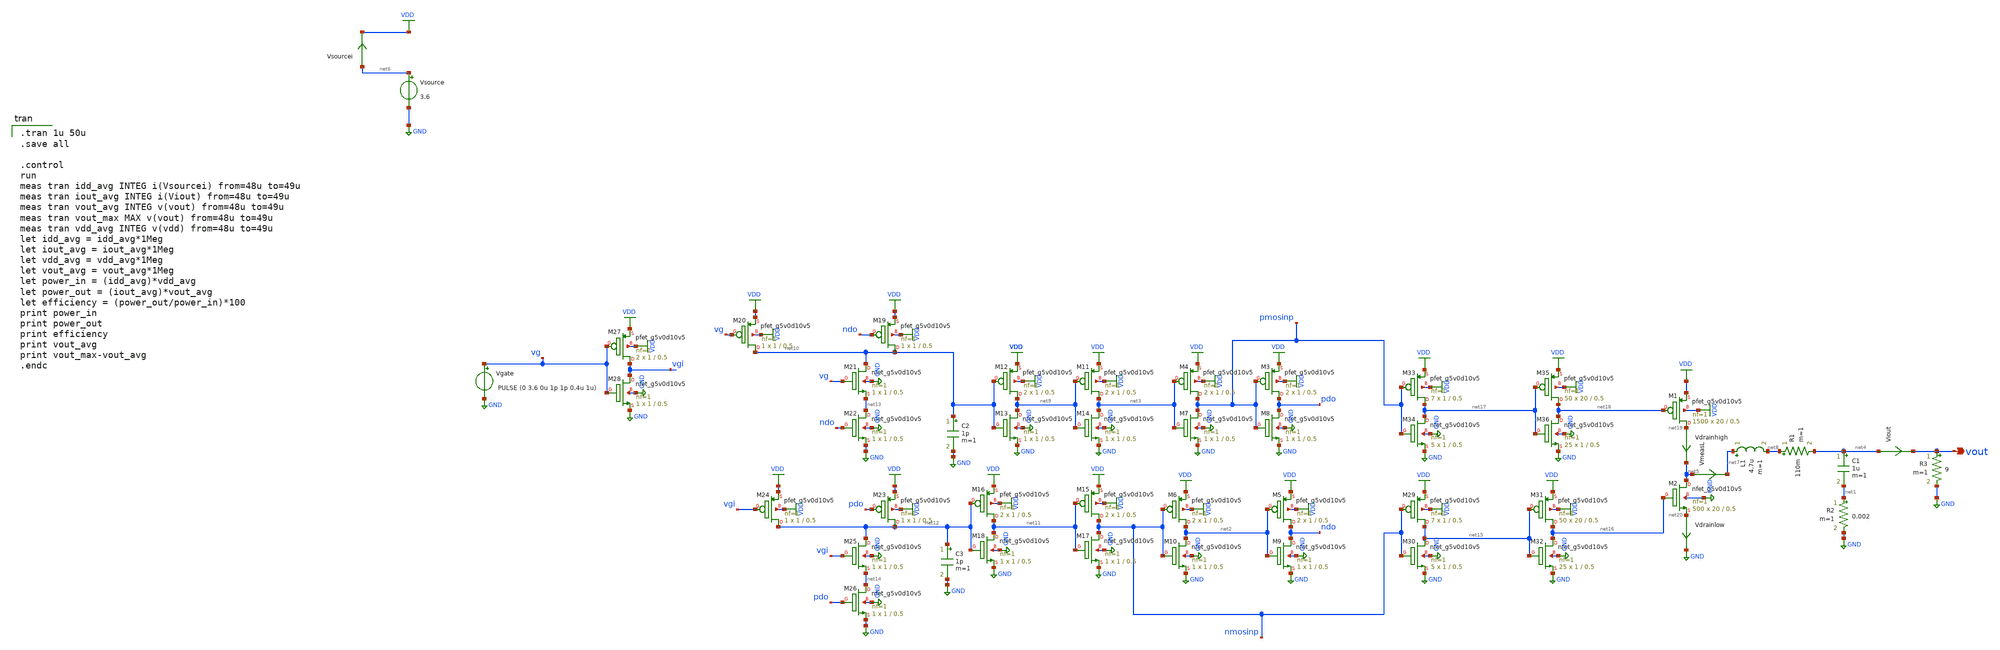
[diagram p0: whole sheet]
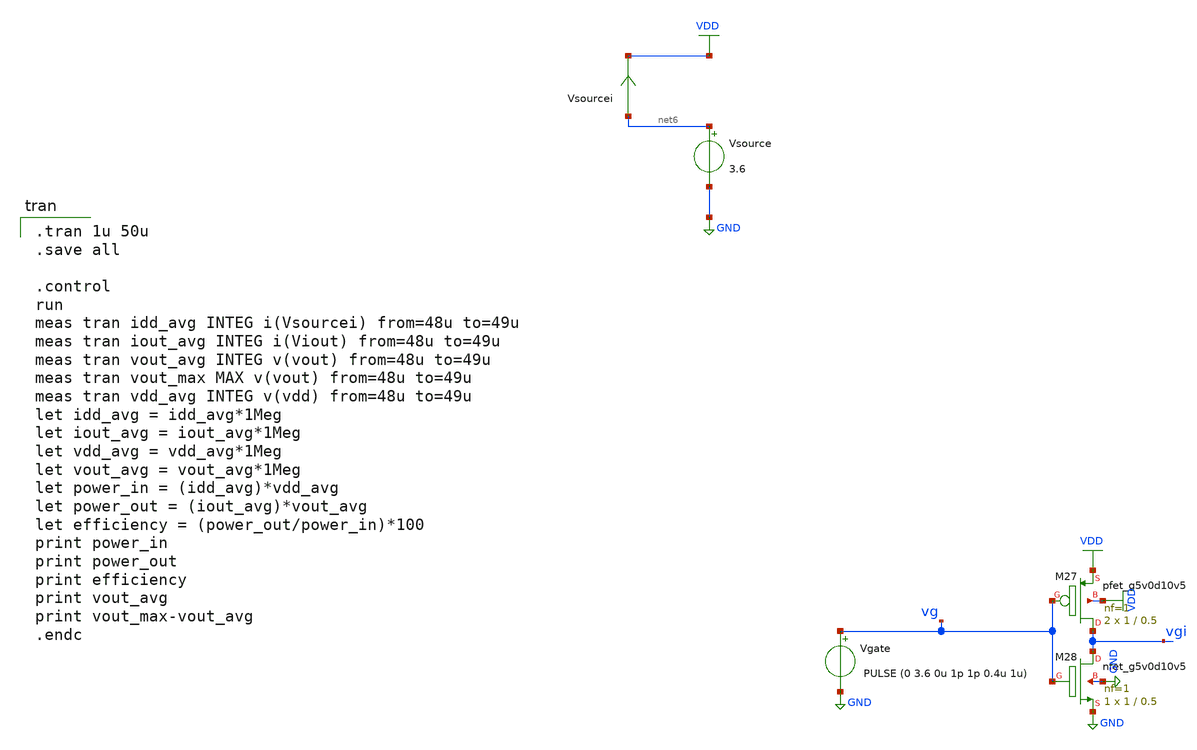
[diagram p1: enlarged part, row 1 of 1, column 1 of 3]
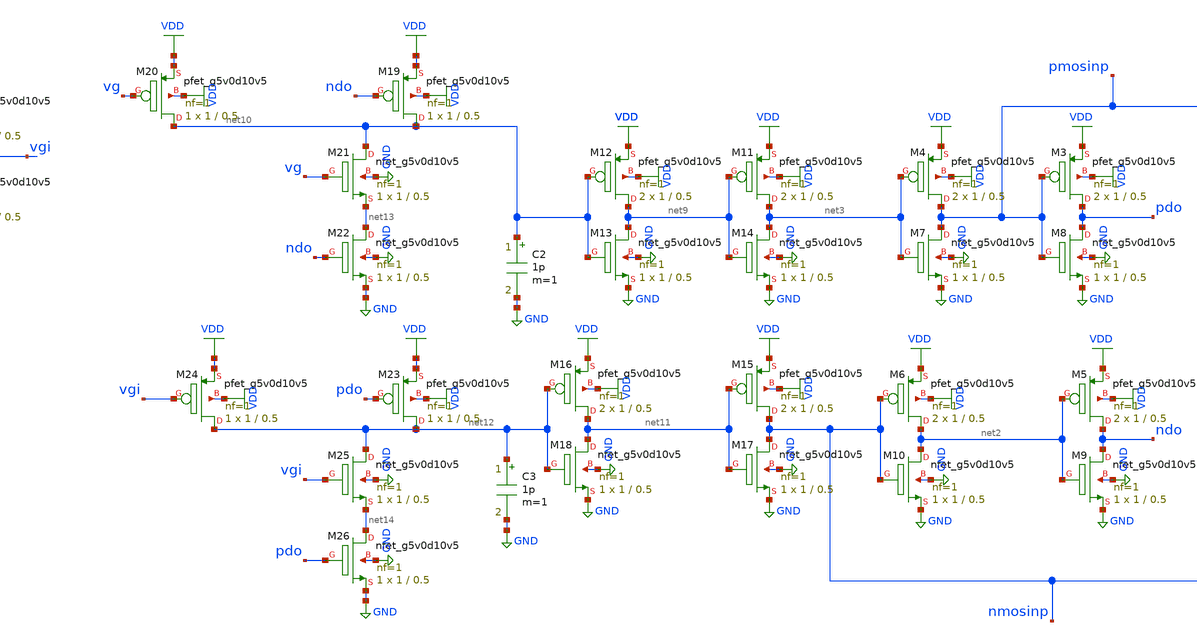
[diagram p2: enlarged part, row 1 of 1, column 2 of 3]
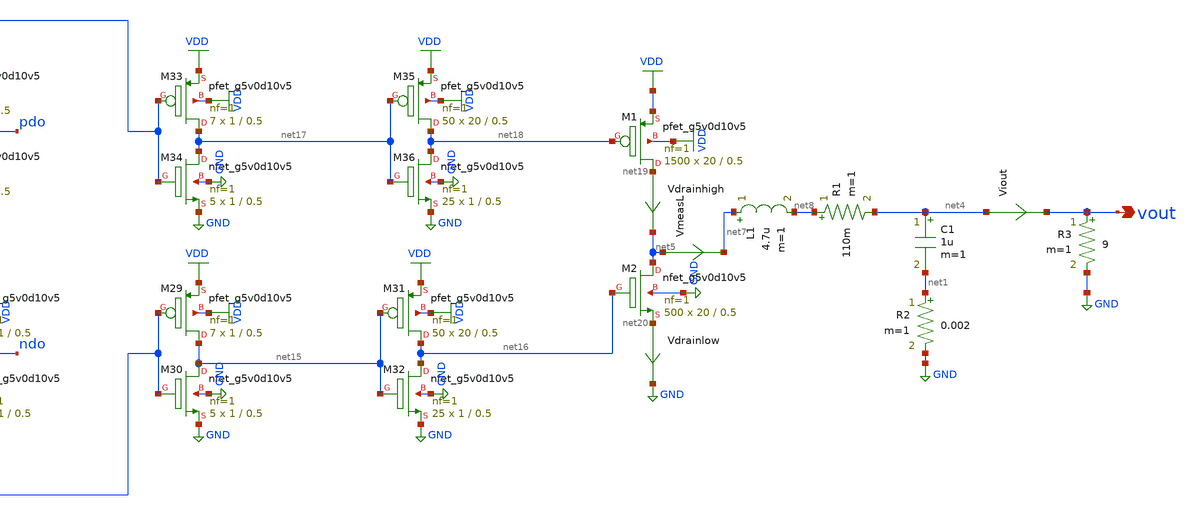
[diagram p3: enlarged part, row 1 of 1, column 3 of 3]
** sch_path: SMPS_With_Deadtime/buck_converter.sch
**.subckt buck_converter vout
*.opin vout
XM1 net19 net18 VDD VDD sky130_fd_pr__pfet_g5v0d10v5 L=0.5 W=20 nf=1 ad='int((nf+1)/2) * W/nf * 0.29'
+ as='int((nf+2)/2) * W/nf * 0.29' pd='2*int((nf+1)/2) * (W/nf + 0.29)' ps='2*int((nf+2)/2) * (W/nf + 0.29)'
+ nrd='0.29 / W' nrs='0.29 / W' sa=0 sb=0 sd=0 mult=1500 m=1500
XM2 net5 net16 net20 GND sky130_fd_pr__nfet_g5v0d10v5 L=0.5 W=20 nf=1 ad='int((nf+1)/2) * W/nf * 0.29'
+ as='int((nf+2)/2) * W/nf * 0.29' pd='2*int((nf+1)/2) * (W/nf + 0.29)' ps='2*int((nf+2)/2) * (W/nf + 0.29)'
+ nrd='0.29 / W' nrs='0.29 / W' sa=0 sb=0 sd=0 mult=500 m=500
L1 net7 net8 4.7u m=1
R1 net8 net4 110m m=1
C1 net4 net1 1u m=1
R2 net1 GND 0.002 m=1
Vgate vg GND PULSE (0 3.6 0u 1p 1p 0.4u 1u)
Vsource net6 GND 3.6
XM3 pdo pmosinp VDD VDD sky130_fd_pr__pfet_g5v0d10v5 L=0.5 W=1 nf=1 ad='int((nf+1)/2) * W/nf * 0.29'
+ as='int((nf+2)/2) * W/nf * 0.29' pd='2*int((nf+1)/2) * (W/nf + 0.29)' ps='2*int((nf+2)/2) * (W/nf + 0.29)'
+ nrd='0.29 / W' nrs='0.29 / W' sa=0 sb=0 sd=0 mult=2 m=2
XM4 pmosinp net3 VDD VDD sky130_fd_pr__pfet_g5v0d10v5 L=0.5 W=1 nf=1 ad='int((nf+1)/2) * W/nf * 0.29'
+ as='int((nf+2)/2) * W/nf * 0.29' pd='2*int((nf+1)/2) * (W/nf + 0.29)' ps='2*int((nf+2)/2) * (W/nf + 0.29)'
+ nrd='0.29 / W' nrs='0.29 / W' sa=0 sb=0 sd=0 mult=2 m=2
XM5 ndo net2 VDD VDD sky130_fd_pr__pfet_g5v0d10v5 L=0.5 W=1 nf=1 ad='int((nf+1)/2) * W/nf * 0.29' as='int((nf+2)/2) * W/nf * 0.29'
+ pd='2*int((nf+1)/2) * (W/nf + 0.29)' ps='2*int((nf+2)/2) * (W/nf + 0.29)' nrd='0.29 / W' nrs='0.29 / W'
+ sa=0 sb=0 sd=0 mult=2 m=2
XM6 net2 nmosinp VDD VDD sky130_fd_pr__pfet_g5v0d10v5 L=0.5 W=1 nf=1 ad='int((nf+1)/2) * W/nf * 0.29'
+ as='int((nf+2)/2) * W/nf * 0.29' pd='2*int((nf+1)/2) * (W/nf + 0.29)' ps='2*int((nf+2)/2) * (W/nf + 0.29)'
+ nrd='0.29 / W' nrs='0.29 / W' sa=0 sb=0 sd=0 mult=2 m=2
XM7 pmosinp net3 GND GND sky130_fd_pr__nfet_g5v0d10v5 L=0.5 W=1 nf=1 ad='int((nf+1)/2) * W/nf * 0.29'
+ as='int((nf+2)/2) * W/nf * 0.29' pd='2*int((nf+1)/2) * (W/nf + 0.29)' ps='2*int((nf+2)/2) * (W/nf + 0.29)'
+ nrd='0.29 / W' nrs='0.29 / W' sa=0 sb=0 sd=0 mult=1 m=1
XM8 pdo pmosinp GND GND sky130_fd_pr__nfet_g5v0d10v5 L=0.5 W=1 nf=1 ad='int((nf+1)/2) * W/nf * 0.29'
+ as='int((nf+2)/2) * W/nf * 0.29' pd='2*int((nf+1)/2) * (W/nf + 0.29)' ps='2*int((nf+2)/2) * (W/nf + 0.29)'
+ nrd='0.29 / W' nrs='0.29 / W' sa=0 sb=0 sd=0 mult=1 m=1
XM9 ndo net2 GND GND sky130_fd_pr__nfet_g5v0d10v5 L=0.5 W=1 nf=1 ad='int((nf+1)/2) * W/nf * 0.29' as='int((nf+2)/2) * W/nf * 0.29'
+ pd='2*int((nf+1)/2) * (W/nf + 0.29)' ps='2*int((nf+2)/2) * (W/nf + 0.29)' nrd='0.29 / W' nrs='0.29 / W'
+ sa=0 sb=0 sd=0 mult=1 m=1
XM10 net2 nmosinp GND GND sky130_fd_pr__nfet_g5v0d10v5 L=0.5 W=1 nf=1 ad='int((nf+1)/2) * W/nf * 0.29'
+ as='int((nf+2)/2) * W/nf * 0.29' pd='2*int((nf+1)/2) * (W/nf + 0.29)' ps='2*int((nf+2)/2) * (W/nf + 0.29)'
+ nrd='0.29 / W' nrs='0.29 / W' sa=0 sb=0 sd=0 mult=1 m=1
Vdrainhigh net19 net5 0
.save i(vdrainhigh)
Viout net4 vout 0
.save i(viout)
R3 vout GND 9 m=1
Vsourcei net6 VDD 0
.save i(vsourcei)
VmeasL net5 net7 0
.save i(vmeasl)
XM11 net3 net9 VDD VDD sky130_fd_pr__pfet_g5v0d10v5 L=0.5 W=1 nf=1 ad='int((nf+1)/2) * W/nf * 0.29' as='int((nf+2)/2) * W/nf * 0.29'
+ pd='2*int((nf+1)/2) * (W/nf + 0.29)' ps='2*int((nf+2)/2) * (W/nf + 0.29)' nrd='0.29 / W' nrs='0.29 / W'
+ sa=0 sb=0 sd=0 mult=2 m=2
XM12 net9 net10 VDD VDD sky130_fd_pr__pfet_g5v0d10v5 L=0.5 W=1 nf=1 ad='int((nf+1)/2) * W/nf * 0.29'
+ as='int((nf+2)/2) * W/nf * 0.29' pd='2*int((nf+1)/2) * (W/nf + 0.29)' ps='2*int((nf+2)/2) * (W/nf + 0.29)'
+ nrd='0.29 / W' nrs='0.29 / W' sa=0 sb=0 sd=0 mult=2 m=2
XM13 net9 net10 GND GND sky130_fd_pr__nfet_g5v0d10v5 L=0.5 W=1 nf=1 ad='int((nf+1)/2) * W/nf * 0.29'
+ as='int((nf+2)/2) * W/nf * 0.29' pd='2*int((nf+1)/2) * (W/nf + 0.29)' ps='2*int((nf+2)/2) * (W/nf + 0.29)'
+ nrd='0.29 / W' nrs='0.29 / W' sa=0 sb=0 sd=0 mult=1 m=1
XM14 net3 net9 GND GND sky130_fd_pr__nfet_g5v0d10v5 L=0.5 W=1 nf=1 ad='int((nf+1)/2) * W/nf * 0.29' as='int((nf+2)/2) * W/nf * 0.29'
+ pd='2*int((nf+1)/2) * (W/nf + 0.29)' ps='2*int((nf+2)/2) * (W/nf + 0.29)' nrd='0.29 / W' nrs='0.29 / W'
+ sa=0 sb=0 sd=0 mult=1 m=1
XM15 nmosinp net11 VDD VDD sky130_fd_pr__pfet_g5v0d10v5 L=0.5 W=1 nf=1 ad='int((nf+1)/2) * W/nf * 0.29'
+ as='int((nf+2)/2) * W/nf * 0.29' pd='2*int((nf+1)/2) * (W/nf + 0.29)' ps='2*int((nf+2)/2) * (W/nf + 0.29)'
+ nrd='0.29 / W' nrs='0.29 / W' sa=0 sb=0 sd=0 mult=2 m=2
XM16 net11 net12 VDD VDD sky130_fd_pr__pfet_g5v0d10v5 L=0.5 W=1 nf=1 ad='int((nf+1)/2) * W/nf * 0.29'
+ as='int((nf+2)/2) * W/nf * 0.29' pd='2*int((nf+1)/2) * (W/nf + 0.29)' ps='2*int((nf+2)/2) * (W/nf + 0.29)'
+ nrd='0.29 / W' nrs='0.29 / W' sa=0 sb=0 sd=0 mult=2 m=2
XM17 nmosinp net11 GND GND sky130_fd_pr__nfet_g5v0d10v5 L=0.5 W=1 nf=1 ad='int((nf+1)/2) * W/nf * 0.29'
+ as='int((nf+2)/2) * W/nf * 0.29' pd='2*int((nf+1)/2) * (W/nf + 0.29)' ps='2*int((nf+2)/2) * (W/nf + 0.29)'
+ nrd='0.29 / W' nrs='0.29 / W' sa=0 sb=0 sd=0 mult=1 m=1
XM18 net11 net12 GND GND sky130_fd_pr__nfet_g5v0d10v5 L=0.5 W=1 nf=1 ad='int((nf+1)/2) * W/nf * 0.29'
+ as='int((nf+2)/2) * W/nf * 0.29' pd='2*int((nf+1)/2) * (W/nf + 0.29)' ps='2*int((nf+2)/2) * (W/nf + 0.29)'
+ nrd='0.29 / W' nrs='0.29 / W' sa=0 sb=0 sd=0 mult=1 m=1
XM19 net10 ndo VDD VDD sky130_fd_pr__pfet_g5v0d10v5 L=0.5 W=1 nf=1 ad='int((nf+1)/2) * W/nf * 0.29' as='int((nf+2)/2) * W/nf * 0.29'
+ pd='2*int((nf+1)/2) * (W/nf + 0.29)' ps='2*int((nf+2)/2) * (W/nf + 0.29)' nrd='0.29 / W' nrs='0.29 / W'
+ sa=0 sb=0 sd=0 mult=1 m=1
XM20 net10 vg VDD VDD sky130_fd_pr__pfet_g5v0d10v5 L=0.5 W=1 nf=1 ad='int((nf+1)/2) * W/nf * 0.29' as='int((nf+2)/2) * W/nf * 0.29'
+ pd='2*int((nf+1)/2) * (W/nf + 0.29)' ps='2*int((nf+2)/2) * (W/nf + 0.29)' nrd='0.29 / W' nrs='0.29 / W'
+ sa=0 sb=0 sd=0 mult=1 m=1
XM21 net10 vg net13 GND sky130_fd_pr__nfet_g5v0d10v5 L=0.5 W=1 nf=1 ad='int((nf+1)/2) * W/nf * 0.29'
+ as='int((nf+2)/2) * W/nf * 0.29' pd='2*int((nf+1)/2) * (W/nf + 0.29)' ps='2*int((nf+2)/2) * (W/nf + 0.29)'
+ nrd='0.29 / W' nrs='0.29 / W' sa=0 sb=0 sd=0 mult=1 m=1
XM22 net13 ndo GND GND sky130_fd_pr__nfet_g5v0d10v5 L=0.5 W=1 nf=1 ad='int((nf+1)/2) * W/nf * 0.29' as='int((nf+2)/2) * W/nf * 0.29'
+ pd='2*int((nf+1)/2) * (W/nf + 0.29)' ps='2*int((nf+2)/2) * (W/nf + 0.29)' nrd='0.29 / W' nrs='0.29 / W'
+ sa=0 sb=0 sd=0 mult=1 m=1
XM23 net12 pdo VDD VDD sky130_fd_pr__pfet_g5v0d10v5 L=0.5 W=1 nf=1 ad='int((nf+1)/2) * W/nf * 0.29' as='int((nf+2)/2) * W/nf * 0.29'
+ pd='2*int((nf+1)/2) * (W/nf + 0.29)' ps='2*int((nf+2)/2) * (W/nf + 0.29)' nrd='0.29 / W' nrs='0.29 / W'
+ sa=0 sb=0 sd=0 mult=1 m=1
XM25 net12 vgi net14 GND sky130_fd_pr__nfet_g5v0d10v5 L=0.5 W=1 nf=1 ad='int((nf+1)/2) * W/nf * 0.29'
+ as='int((nf+2)/2) * W/nf * 0.29' pd='2*int((nf+1)/2) * (W/nf + 0.29)' ps='2*int((nf+2)/2) * (W/nf + 0.29)'
+ nrd='0.29 / W' nrs='0.29 / W' sa=0 sb=0 sd=0 mult=1 m=1
XM26 net14 pdo GND GND sky130_fd_pr__nfet_g5v0d10v5 L=0.5 W=1 nf=1 ad='int((nf+1)/2) * W/nf * 0.29' as='int((nf+2)/2) * W/nf * 0.29'
+ pd='2*int((nf+1)/2) * (W/nf + 0.29)' ps='2*int((nf+2)/2) * (W/nf + 0.29)' nrd='0.29 / W' nrs='0.29 / W'
+ sa=0 sb=0 sd=0 mult=1 m=1
XM27 vgi vg VDD VDD sky130_fd_pr__pfet_g5v0d10v5 L=0.5 W=1 nf=1 ad='int((nf+1)/2) * W/nf * 0.29' as='int((nf+2)/2) * W/nf * 0.29'
+ pd='2*int((nf+1)/2) * (W/nf + 0.29)' ps='2*int((nf+2)/2) * (W/nf + 0.29)' nrd='0.29 / W' nrs='0.29 / W'
+ sa=0 sb=0 sd=0 mult=2 m=2
XM28 vgi vg GND GND sky130_fd_pr__nfet_g5v0d10v5 L=0.5 W=1 nf=1 ad='int((nf+1)/2) * W/nf * 0.29' as='int((nf+2)/2) * W/nf * 0.29'
+ pd='2*int((nf+1)/2) * (W/nf + 0.29)' ps='2*int((nf+2)/2) * (W/nf + 0.29)' nrd='0.29 / W' nrs='0.29 / W'
+ sa=0 sb=0 sd=0 mult=1 m=1
C2 net10 GND 1p m=1
C3 net12 GND 1p m=1
XM24 net12 vgi VDD VDD sky130_fd_pr__pfet_g5v0d10v5 L=0.5 W=1 nf=1 ad='int((nf+1)/2) * W/nf * 0.29' as='int((nf+2)/2) * W/nf * 0.29'
+ pd='2*int((nf+1)/2) * (W/nf + 0.29)' ps='2*int((nf+2)/2) * (W/nf + 0.29)' nrd='0.29 / W' nrs='0.29 / W'
+ sa=0 sb=0 sd=0 mult=1 m=1
XM29 net15 nmosinp VDD VDD sky130_fd_pr__pfet_g5v0d10v5 L=0.5 W=1 nf=1 ad='int((nf+1)/2) * W/nf * 0.29'
+ as='int((nf+2)/2) * W/nf * 0.29' pd='2*int((nf+1)/2) * (W/nf + 0.29)' ps='2*int((nf+2)/2) * (W/nf + 0.29)'
+ nrd='0.29 / W' nrs='0.29 / W' sa=0 sb=0 sd=0 mult=7 m=7
XM30 net15 nmosinp GND GND sky130_fd_pr__nfet_g5v0d10v5 L=0.5 W=1 nf=1 ad='int((nf+1)/2) * W/nf * 0.29'
+ as='int((nf+2)/2) * W/nf * 0.29' pd='2*int((nf+1)/2) * (W/nf + 0.29)' ps='2*int((nf+2)/2) * (W/nf + 0.29)'
+ nrd='0.29 / W' nrs='0.29 / W' sa=0 sb=0 sd=0 mult=5 m=5
XM31 net16 net15 VDD VDD sky130_fd_pr__pfet_g5v0d10v5 L=0.5 W=20 nf=1 ad='int((nf+1)/2) * W/nf * 0.29'
+ as='int((nf+2)/2) * W/nf * 0.29' pd='2*int((nf+1)/2) * (W/nf + 0.29)' ps='2*int((nf+2)/2) * (W/nf + 0.29)'
+ nrd='0.29 / W' nrs='0.29 / W' sa=0 sb=0 sd=0 mult=50 m=50
XM32 net16 net15 GND GND sky130_fd_pr__nfet_g5v0d10v5 L=0.5 W=1 nf=1 ad='int((nf+1)/2) * W/nf * 0.29'
+ as='int((nf+2)/2) * W/nf * 0.29' pd='2*int((nf+1)/2) * (W/nf + 0.29)' ps='2*int((nf+2)/2) * (W/nf + 0.29)'
+ nrd='0.29 / W' nrs='0.29 / W' sa=0 sb=0 sd=0 mult=25 m=25
XM33 net17 pmosinp VDD VDD sky130_fd_pr__pfet_g5v0d10v5 L=0.5 W=1 nf=1 ad='int((nf+1)/2) * W/nf * 0.29'
+ as='int((nf+2)/2) * W/nf * 0.29' pd='2*int((nf+1)/2) * (W/nf + 0.29)' ps='2*int((nf+2)/2) * (W/nf + 0.29)'
+ nrd='0.29 / W' nrs='0.29 / W' sa=0 sb=0 sd=0 mult=7 m=7
XM34 net17 pmosinp GND GND sky130_fd_pr__nfet_g5v0d10v5 L=0.5 W=1 nf=1 ad='int((nf+1)/2) * W/nf * 0.29'
+ as='int((nf+2)/2) * W/nf * 0.29' pd='2*int((nf+1)/2) * (W/nf + 0.29)' ps='2*int((nf+2)/2) * (W/nf + 0.29)'
+ nrd='0.29 / W' nrs='0.29 / W' sa=0 sb=0 sd=0 mult=5 m=5
XM35 net18 net17 VDD VDD sky130_fd_pr__pfet_g5v0d10v5 L=0.5 W=20 nf=1 ad='int((nf+1)/2) * W/nf * 0.29'
+ as='int((nf+2)/2) * W/nf * 0.29' pd='2*int((nf+1)/2) * (W/nf + 0.29)' ps='2*int((nf+2)/2) * (W/nf + 0.29)'
+ nrd='0.29 / W' nrs='0.29 / W' sa=0 sb=0 sd=0 mult=50 m=50
XM36 net18 net17 GND GND sky130_fd_pr__nfet_g5v0d10v5 L=0.5 W=1 nf=1 ad='int((nf+1)/2) * W/nf * 0.29'
+ as='int((nf+2)/2) * W/nf * 0.29' pd='2*int((nf+1)/2) * (W/nf + 0.29)' ps='2*int((nf+2)/2) * (W/nf + 0.29)'
+ nrd='0.29 / W' nrs='0.29 / W' sa=0 sb=0 sd=0 mult=25 m=25
Vdrainlow net20 GND 0
.save i(vdrainlow)
**** begin user architecture code
  .lib $::SKYWATER_MODELS/sky130.lib.spice tt

.tran 1u 50u
.save all

.control
run
meas tran idd_avg INTEG i(Vsourcei) from=48u to=49u
meas tran iout_avg INTEG i(Viout) from=48u to=49u
meas tran vout_avg INTEG v(vout) from=48u to=49u
meas tran vout_max MAX v(vout) from=48u to=49u
meas tran vdd_avg INTEG v(vdd) from=48u to=49u
let idd_avg = idd_avg*1Meg
let iout_avg = iout_avg*1Meg
let vdd_avg = vdd_avg*1Meg
let vout_avg = vout_avg*1Meg
let power_in = (idd_avg)*vdd_avg
let power_out = (iout_avg)*vout_avg
let efficiency = (power_out/power_in)*100
print power_in
print power_out
print efficiency
print vout_avg
print vout_max-vout_avg
.endc










**** end user architecture code
**.ends
.GLOBAL VDD
.GLOBAL GND
.end
